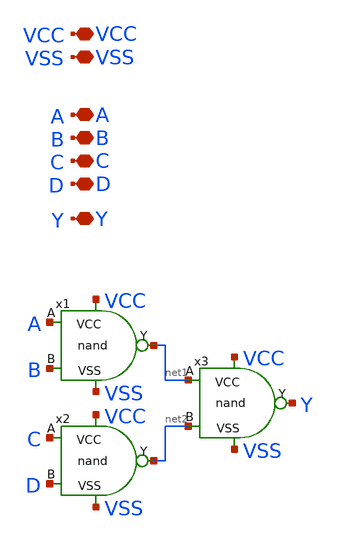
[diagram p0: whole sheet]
** sch_path: logic gates/nand4.sch
**.subckt nand4 A B C D Y VCC VSS
*.iopin A
*.iopin B
*.iopin C
*.iopin D
*.iopin Y
*.iopin VCC
*.iopin VSS
x1 VCC net1 A B VSS nand
x2 VCC net2 C D VSS nand
x3 VCC Y net1 net2 VSS nand
**.ends

* expanding   symbol:  logic gates/nand.sym # of pins=5
** sym_path: logic gates/nand.sym
** sch_path: logic gates/nand.sch
.subckt nand VCC Y A B VSS
*.iopin VCC
*.iopin VSS
*.iopin Y
*.iopin A
*.iopin B
XM2 net1 B VSS VSS sky130_fd_pr__nfet_01v8 L=0.15 W=1 nf=1 ad='int((1 + 1)/2) * 1 / 1 * 0.29' as='int((1 + 2)/2) * 1 / 1 * 0.29'
+ pd='2*int((1 + 1)/2) * (1 / 1 + 0.29)' ps='2*int((1 + 2)/2) * (1 / 1 + 0.29)' nrd='0.29 / 1 ' nrs='0.29 / 1 '
+ sa=0 sb=0 sd=0 mult=1 m=1
XM11 Y A VCC VCC sky130_fd_pr__pfet_01v8 L=0.15 W=1 nf=1 ad='int((nf+1)/2) * W/nf * 0.29' as='int((nf+2)/2) * W/nf * 0.29'
+ pd='2*int((nf+1)/2) * (W/nf + 0.29)' ps='2*int((nf+2)/2) * (W/nf + 0.29)' nrd='0.29 / W' nrs='0.29 / W'
+ sa=0 sb=0 sd=0 mult=1 m=1
XM1 Y A net1 VSS sky130_fd_pr__nfet_01v8 L=0.15 W=1 nf=1 ad='int((1 + 1)/2) * 1 / 1 * 0.29' as='int((1 + 2)/2) * 1 / 1 * 0.29'
+ pd='2*int((1 + 1)/2) * (1 / 1 + 0.29)' ps='2*int((1 + 2)/2) * (1 / 1 + 0.29)' nrd='0.29 / 1 ' nrs='0.29 / 1 '
+ sa=0 sb=0 sd=0 mult=1 m=1
XM3 Y B VCC VCC sky130_fd_pr__pfet_01v8 L=0.15 W=1 nf=1 ad='int((nf+1)/2) * W/nf * 0.29' as='int((nf+2)/2) * W/nf * 0.29'
+ pd='2*int((nf+1)/2) * (W/nf + 0.29)' ps='2*int((nf+2)/2) * (W/nf + 0.29)' nrd='0.29 / W' nrs='0.29 / W'
+ sa=0 sb=0 sd=0 mult=1 m=1
.ends

.end
